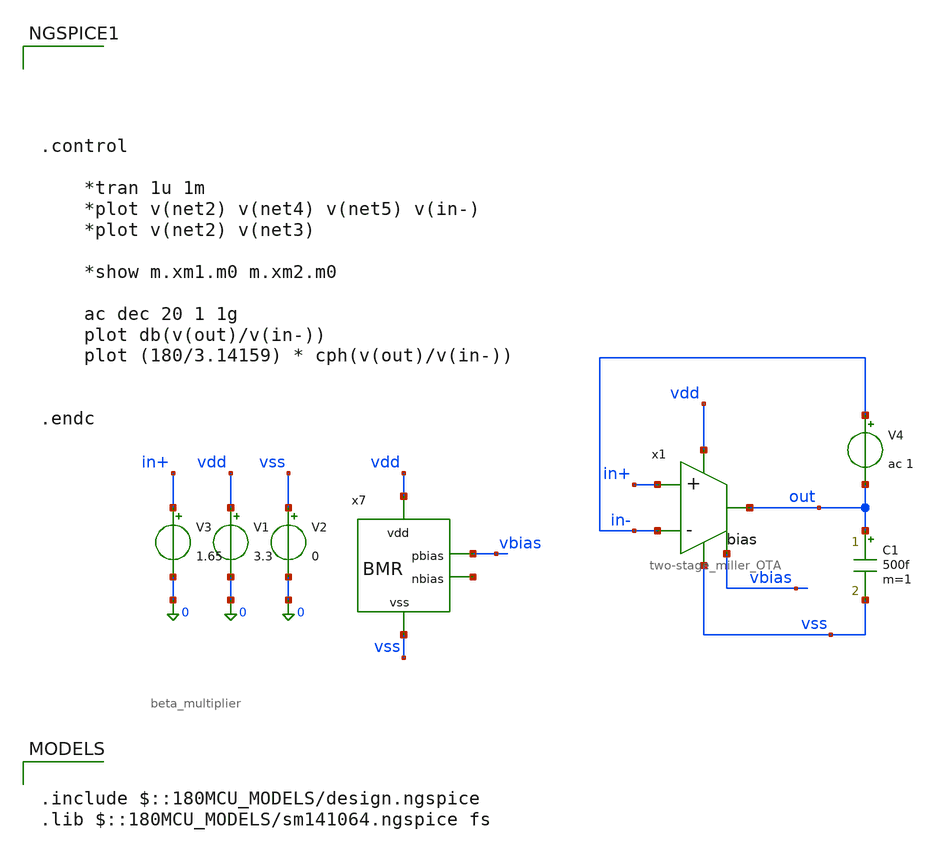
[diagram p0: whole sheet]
** sch_path: simulation/testbench_analog/OTA/OTA_freq-response.sch
**.subckt OTA_freq-response
V3 in+ 0 1.65
V1 vdd 0 3.3
V2 vss 0 0
x1 vdd out in+ in- vbias vss two-stage_miller_OTA
V4 in- out ac 1
C1 out vss 500f m=1
x7 vdd vbias net1 vss beta_multiplier
**** begin user architecture code





.control

	*tran 1u 1m
	*plot v(net2) v(net4) v(net5) v(in-)
	*plot v(net2) v(net3)

	*show m.xm1.m0 m.xm2.m0

	ac dec 20 1 1g
	plot db(v(out)/v(in-))
	plot (180/3.14159) * cph(v(out)/v(in-))


.endc



.include $::180MCU_MODELS/design.ngspice
.lib $::180MCU_MODELS/sm141064.ngspice fs

**** end user architecture code
**.ends

* expanding   symbol:  acoustic_ranger_2026/two-stage_miller_OTA.sym # of pins=6
** sym_path: design/analog/OTA/two-stage_miller_OTA.sym
** sch_path: design/analog/OTA/two-stage_miller_OTA.sch
.subckt two-stage_miller_OTA vdd out in+ in- bias vss
*.ipin in+
*.ipin in-
*.opin out
*.iopin vdd
*.iopin vss
*.ipin bias
XM1 net2 in- net1 vdd pfet_03v3 L=1u W=6.2u nf=1 ad='int((nf+1)/2) * W/nf * 0.18u' as='int((nf+2)/2) * W/nf * 0.18u'
+ pd='2*int((nf+1)/2) * (W/nf + 0.18u)' ps='2*int((nf+2)/2) * (W/nf + 0.18u)' nrd='0.18u / W' nrs='0.18u / W'
+ sa=0 sb=0 sd=0 m=8
XM2 net3 in+ net1 vdd pfet_03v3 L=1u W=6.2u nf=1 ad='int((nf+1)/2) * W/nf * 0.18u' as='int((nf+2)/2) * W/nf * 0.18u'
+ pd='2*int((nf+1)/2) * (W/nf + 0.18u)' ps='2*int((nf+2)/2) * (W/nf + 0.18u)' nrd='0.18u / W' nrs='0.18u / W'
+ sa=0 sb=0 sd=0 m=8
XM14 net3 net2 vss vss nfet_03v3 L=3u W=7.7u nf=4 ad='int((nf+1)/2) * W/nf * 0.18u' as='int((nf+2)/2) * W/nf * 0.18u'
+ pd='2*int((nf+1)/2) * (W/nf + 0.18u)' ps='2*int((nf+2)/2) * (W/nf + 0.18u)' nrd='0.18u / W' nrs='0.18u / W'
+ sa=0 sb=0 sd=0 m=2
XM15 net2 net2 vss vss nfet_03v3 L=3u W=7.7u nf=4 ad='int((nf+1)/2) * W/nf * 0.18u' as='int((nf+2)/2) * W/nf * 0.18u'
+ pd='2*int((nf+1)/2) * (W/nf + 0.18u)' ps='2*int((nf+2)/2) * (W/nf + 0.18u)' nrd='0.18u / W' nrs='0.18u / W'
+ sa=0 sb=0 sd=0 m=2
XM3 out net3 vss vss nfet_03v3 L=3u W=7.7u nf=4 ad='int((nf+1)/2) * W/nf * 0.18u' as='int((nf+2)/2) * W/nf * 0.18u'
+ pd='2*int((nf+1)/2) * (W/nf + 0.18u)' ps='2*int((nf+2)/2) * (W/nf + 0.18u)' nrd='0.18u / W' nrs='0.18u / W'
+ sa=0 sb=0 sd=0 m=12
C1 out net3 5p m=1
XM4 net1 bias vdd vdd pfet_03v3 L=20u W=25.3u nf=2 ad='int((nf+1)/2) * W/nf * 0.18u' as='int((nf+2)/2) * W/nf * 0.18u'
+ pd='2*int((nf+1)/2) * (W/nf + 0.18u)' ps='2*int((nf+2)/2) * (W/nf + 0.18u)' nrd='0.18u / W' nrs='0.18u / W'
+ sa=0 sb=0 sd=0 m=2
XM5 out bias vdd vdd pfet_03v3 L=20u W=25.3u nf=2 ad='int((nf+1)/2) * W/nf * 0.18u' as='int((nf+2)/2) * W/nf * 0.18u'
+ pd='2*int((nf+1)/2) * (W/nf + 0.18u)' ps='2*int((nf+2)/2) * (W/nf + 0.18u)' nrd='0.18u / W' nrs='0.18u / W'
+ sa=0 sb=0 sd=0 m=6
.ends


* expanding   symbol:  acoustic-ranger-dvl-processor/design/analog/beta
*+ multiplier/beta_multiplier.sym # of pins=4
** sym_path: design/analog/beta multiplier/beta_multiplier.sym
** sch_path: design/analog/beta multiplier/beta_multiplier.sch
.subckt beta_multiplier vdd pbias nbias vss
*.iopin vdd
*.iopin vss
*.opin pbias
*.opin nbias
XM14 pbias nbias net1 net1 nfet_03v3 L=10u W=13.8u nf=1 ad='int((nf+1)/2) * W/nf * 0.18u' as='int((nf+2)/2) * W/nf * 0.18u'
+ pd='2*int((nf+1)/2) * (W/nf + 0.18u)' ps='2*int((nf+2)/2) * (W/nf + 0.18u)' nrd='0.18u / W' nrs='0.18u / W'
+ sa=0 sb=0 sd=0 m=1
XM15 nbias nbias vss vss nfet_03v3 L=10u W=5.71u nf=1 ad='int((nf+1)/2) * W/nf * 0.18u' as='int((nf+2)/2) * W/nf * 0.18u'
+ pd='2*int((nf+1)/2) * (W/nf + 0.18u)' ps='2*int((nf+2)/2) * (W/nf + 0.18u)' nrd='0.18u / W' nrs='0.18u / W'
+ sa=0 sb=0 sd=0 m=1
XM16 pbias pbias vdd vdd pfet_03v3 L=10u W=40u nf=1 ad='int((nf+1)/2) * W/nf * 0.18u' as='int((nf+2)/2) * W/nf * 0.18u'
+ pd='2*int((nf+1)/2) * (W/nf + 0.18u)' ps='2*int((nf+2)/2) * (W/nf + 0.18u)' nrd='0.18u / W' nrs='0.18u / W'
+ sa=0 sb=0 sd=0 m=1
XM17 nbias pbias vdd vdd pfet_03v3 L=10u W=40u nf=1 ad='int((nf+1)/2) * W/nf * 0.18u' as='int((nf+2)/2) * W/nf * 0.18u'
+ pd='2*int((nf+1)/2) * (W/nf + 0.18u)' ps='2*int((nf+2)/2) * (W/nf + 0.18u)' nrd='0.18u / W' nrs='0.18u / W'
+ sa=0 sb=0 sd=0 m=1
R3 net1 vss 9.012k m=1
.ends

.end
